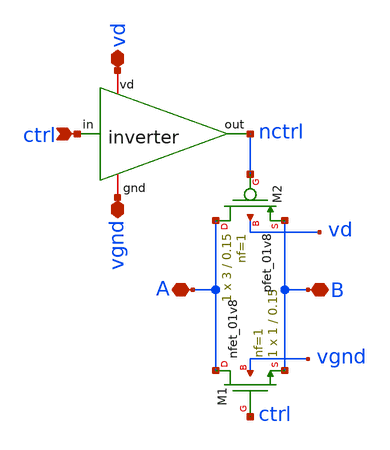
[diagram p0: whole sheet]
** sch_path: .Trash-1000/files/untitled-1.sch
**.subckt untitled-1 B A vgnd vd ctrl
*.iopin B
*.iopin A
*.iopin vgnd
*.iopin vd
*.ipin ctrl
x1 vd ctrl nctrl vgnd inverter
XM1 A ctrl B vgnd sky130_fd_pr__nfet_01v8 L=0.15 W=1 nf=1 ad='int((nf+1)/2) * W/nf * 0.29' as='int((nf+2)/2) * W/nf * 0.29'
+ pd='2*int((nf+1)/2) * (W/nf + 0.29)' ps='2*int((nf+2)/2) * (W/nf + 0.29)' nrd='0.29 / W' nrs='0.29 / W'
+ sa=0 sb=0 sd=0 mult=1 m=1
XM2 A nctrl B vd sky130_fd_pr__pfet_01v8 L=0.15 W=3 nf=1 ad='int((nf+1)/2) * W/nf * 0.29' as='int((nf+2)/2) * W/nf * 0.29'
+ pd='2*int((nf+1)/2) * (W/nf + 0.29)' ps='2*int((nf+2)/2) * (W/nf + 0.29)' nrd='0.29 / W' nrs='0.29 / W'
+ sa=0 sb=0 sd=0 mult=1 m=1
**.ends

* expanding   symbol:  /foss/designs/inverter/xschem_files/inverter.sym # of pins=4
** sym_path: /foss/designs/inverter/xschem_files/inverter.sym
** sch_path: /foss/designs/inverter/xschem_files/inverter.sch
.subckt inverter vd in out gnd
*.ipin in
*.opin out
*.iopin vd
*.iopin gnd
XN0 out in gnd gnd sky130_fd_pr__nfet_01v8 L=0.15 W=1 nf=1 ad='int((nf+1)/2) * W/nf * 0.29' as='int((nf+2)/2) * W/nf * 0.29'
+ pd='2*int((nf+1)/2) * (W/nf + 0.29)' ps='2*int((nf+2)/2) * (W/nf + 0.29)' nrd='0.29 / W' nrs='0.29 / W'
+ sa=0 sb=0 sd=0 mult=1 m=1
XP0 out in vd vd sky130_fd_pr__pfet_01v8 L=0.15 W=3 nf=1 ad='int((nf+1)/2) * W/nf * 0.29' as='int((nf+2)/2) * W/nf * 0.29'
+ pd='2*int((nf+1)/2) * (W/nf + 0.29)' ps='2*int((nf+2)/2) * (W/nf + 0.29)' nrd='0.29 / W' nrs='0.29 / W'
+ sa=0 sb=0 sd=0 mult=1 m=1
.ends

.end
